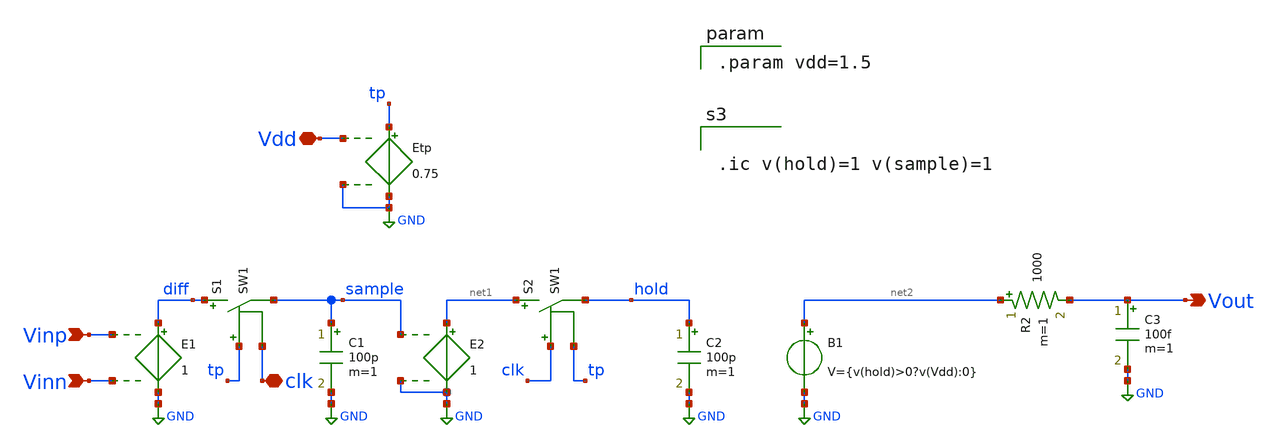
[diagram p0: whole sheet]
** sch_path: DSM_1storder/Schematic_Level/xschem/comparator_newspecs.sch
**.subckt comparator_newspecs Vinp Vinn Vout Vdd clk
*.ipin Vinp
*.ipin Vinn
*.opin Vout
*.iopin Vdd
*.iopin clk
E1 diff GND Vinp Vinn 1
S1 diff sample tp clk SW1
E2 net1 GND sample GND 1
C1 sample GND 100p m=1
S2 net1 hold clk tp SW1
C2 hold GND 100p m=1
B1 net2 GND V={v(hold)>0?v(Vdd):0}
Etp tp GND Vdd GND 0.75
C3 Vout GND 100f m=1
R2 net2 Vout 1000 m=1
**** begin user architecture code


.ic v(hold)=1 v(sample)=1



.param vdd=1.5

**** end user architecture code
**.ends
.GLOBAL GND
**** begin user architecture code
.MODEL SW1 SW( VT=0.4 VH=0.01 RON=0.01 ROFF=10G )
**** end user architecture code
.end
